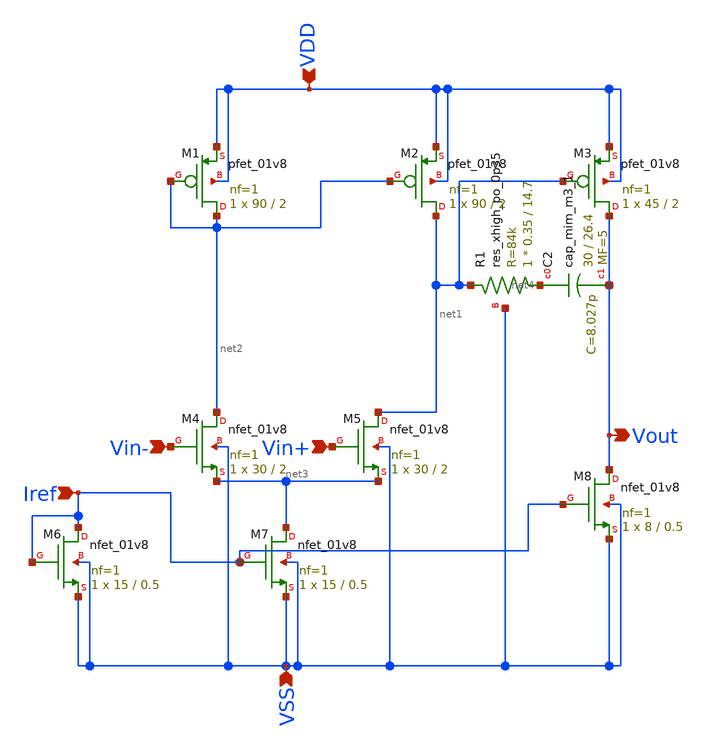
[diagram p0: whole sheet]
** sch_path: schematic/diffpair.sch
**.subckt diffpair Vin+ Iref Vin- Vout VSS VDD
*.ipin Vin+
*.ipin Iref
*.ipin Vin-
*.opin Vout
*.ipin VSS
*.ipin VDD
XC2 net4 Vout sky130_fd_pr__cap_mim_m3_1 W=30 L=26.4 MF=5 m=5
XR1 net4 net1 VSS sky130_fd_pr__res_xhigh_po_0p35 L=14.7 mult=1 m=1
XM1 net2 net2 VDD VDD sky130_fd_pr__pfet_01v8 L=2 W=90 nf=1 ad='int((nf+1)/2) * W/nf * 0.29' as='int((nf+2)/2) * W/nf * 0.29'
+ pd='2*int((nf+1)/2) * (W/nf + 0.29)' ps='2*int((nf+2)/2) * (W/nf + 0.29)' nrd='0.29 / W' nrs='0.29 / W'
+ sa=0 sb=0 sd=0 mult=1 m=1
XM2 net1 net2 VDD VDD sky130_fd_pr__pfet_01v8 L=2 W=90 nf=1 ad='int((nf+1)/2) * W/nf * 0.29' as='int((nf+2)/2) * W/nf * 0.29'
+ pd='2*int((nf+1)/2) * (W/nf + 0.29)' ps='2*int((nf+2)/2) * (W/nf + 0.29)' nrd='0.29 / W' nrs='0.29 / W'
+ sa=0 sb=0 sd=0 mult=1 m=1
XM3 Vout net1 VDD VDD sky130_fd_pr__pfet_01v8 L=2 W=45 nf=1 ad='int((nf+1)/2) * W/nf * 0.29' as='int((nf+2)/2) * W/nf * 0.29'
+ pd='2*int((nf+1)/2) * (W/nf + 0.29)' ps='2*int((nf+2)/2) * (W/nf + 0.29)' nrd='0.29 / W' nrs='0.29 / W'
+ sa=0 sb=0 sd=0 mult=1 m=1
XM4 net2 Vin- net3 VSS sky130_fd_pr__nfet_01v8 L=2 W=30 nf=1 ad='int((nf+1)/2) * W/nf * 0.29' as='int((nf+2)/2) * W/nf * 0.29'
+ pd='2*int((nf+1)/2) * (W/nf + 0.29)' ps='2*int((nf+2)/2) * (W/nf + 0.29)' nrd='0.29 / W' nrs='0.29 / W'
+ sa=0 sb=0 sd=0 mult=1 m=1
XM5 net1 Vin+ net3 VSS sky130_fd_pr__nfet_01v8 L=2 W=30 nf=1 ad='int((nf+1)/2) * W/nf * 0.29' as='int((nf+2)/2) * W/nf * 0.29'
+ pd='2*int((nf+1)/2) * (W/nf + 0.29)' ps='2*int((nf+2)/2) * (W/nf + 0.29)' nrd='0.29 / W' nrs='0.29 / W'
+ sa=0 sb=0 sd=0 mult=1 m=1
XM6 Iref Iref VSS VSS sky130_fd_pr__nfet_01v8 L=0.5 W=15 nf=1 ad='int((nf+1)/2) * W/nf * 0.29' as='int((nf+2)/2) * W/nf * 0.29'
+ pd='2*int((nf+1)/2) * (W/nf + 0.29)' ps='2*int((nf+2)/2) * (W/nf + 0.29)' nrd='0.29 / W' nrs='0.29 / W'
+ sa=0 sb=0 sd=0 mult=1 m=1
XM7 net3 Iref VSS VSS sky130_fd_pr__nfet_01v8 L=0.5 W=15 nf=1 ad='int((nf+1)/2) * W/nf * 0.29' as='int((nf+2)/2) * W/nf * 0.29'
+ pd='2*int((nf+1)/2) * (W/nf + 0.29)' ps='2*int((nf+2)/2) * (W/nf + 0.29)' nrd='0.29 / W' nrs='0.29 / W'
+ sa=0 sb=0 sd=0 mult=1 m=1
XM8 Vout Iref VSS VSS sky130_fd_pr__nfet_01v8 L=0.5 W=8 nf=1 ad='int((nf+1)/2) * W/nf * 0.29' as='int((nf+2)/2) * W/nf * 0.29'
+ pd='2*int((nf+1)/2) * (W/nf + 0.29)' ps='2*int((nf+2)/2) * (W/nf + 0.29)' nrd='0.29 / W' nrs='0.29 / W'
+ sa=0 sb=0 sd=0 mult=1 m=1
**.ends
.end
